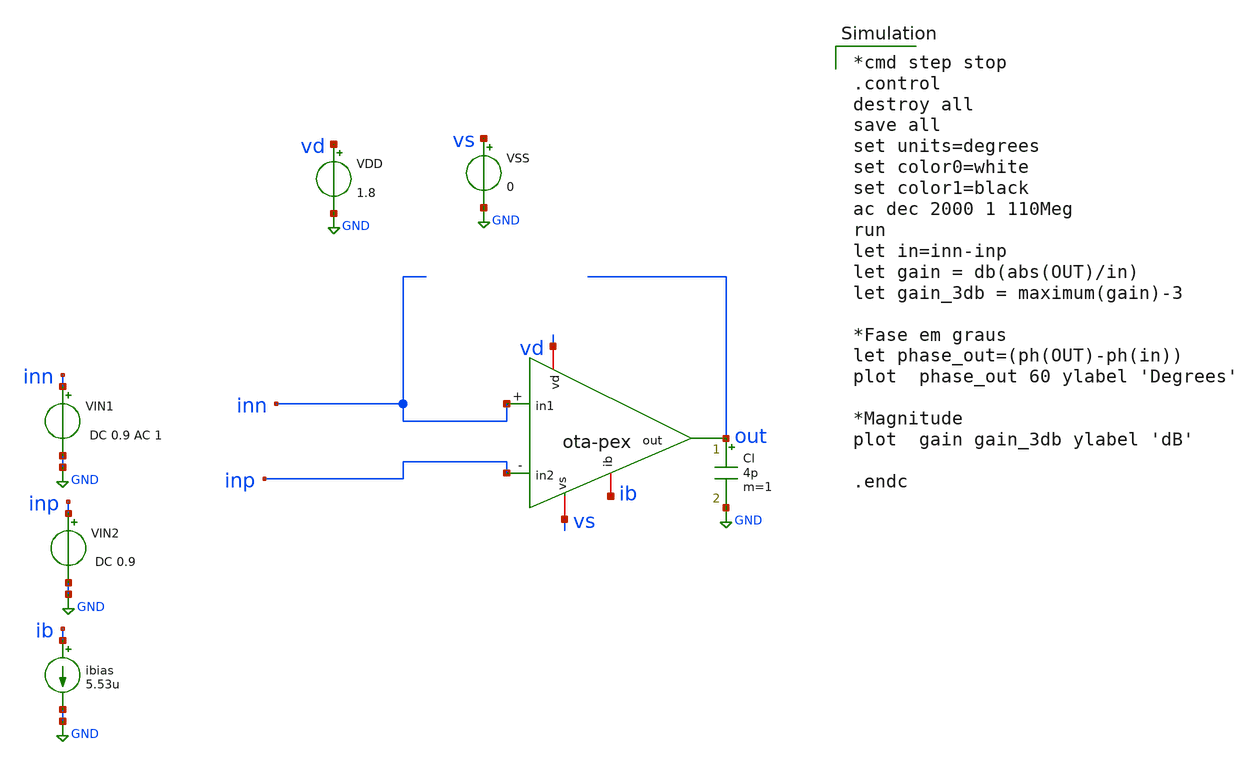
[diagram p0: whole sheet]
** sch_path: ota/xschem/ota_tb-ac.sch
* Copyright 2020 Stefan Frederik Schippers
* Licensed under the Apache License, Version 2.0 (the "License");
* you may not use this file except in compliance with the License.
* You may obtain a copy of the License at
* https://www.apache.org/licenses/LICENSE-2.0
* Unless required by applicable law or agreed to in writing, software
* distributed under the License is distributed on an "AS IS" BASIS,
* WITHOUT WARRANTIES OR CONDITIONS OF ANY KIND, either express or implied.
* See the License for the specific language governing permissions and
* limitations under the License.
**.subckt ota_tb-ac
VIN1 inn GND DC 0.9 AC 1
ibias ib GND 5.53u
VDD vd GND 1.8
VSS vs GND 0
Cl out GND 4p m=1
VIN2 inp GND DC 0.9
X1 vd ib out inp inn vs ota-pex
**** begin user architecture code

*cmd step stop
.control
destroy all
save all
set units=degrees
set color0=white
set color1=black
ac dec 2000 1 110Meg
run
let in=inn-inp
let gain = db(abs(OUT)/in)
let gain_3db = maximum(gain)-3

*Fase em graus
let phase_out=(ph(OUT)-ph(in))
plot  phase_out 60 ylabel 'Degrees'

*Magnitude
plot  gain gain_3db ylabel 'dB'

.endc

 .lib $::SKYWATER_MODELS/sky130.lib.spice tt
.include $::SKYWATER_STDCELLS/sky130_fd_sc_hd.spice

**** end user architecture code
**.ends
.GLOBAL GND
.end
